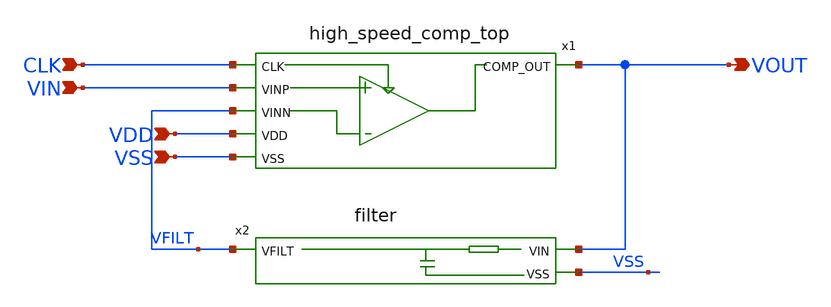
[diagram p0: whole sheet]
** sch_path: xschem/1bit_frontend.sch
**.subckt 1bit_frontend CLK VIN VDD VSS VOUT
*.ipin CLK
*.ipin VIN
*.ipin VDD
*.ipin VSS
*.opin VOUT
x1 CLK VIN VFILT VDD VOUT VSS high_speed_comp_top
x2 VOUT VFILT VSS filter
**.ends
.end
